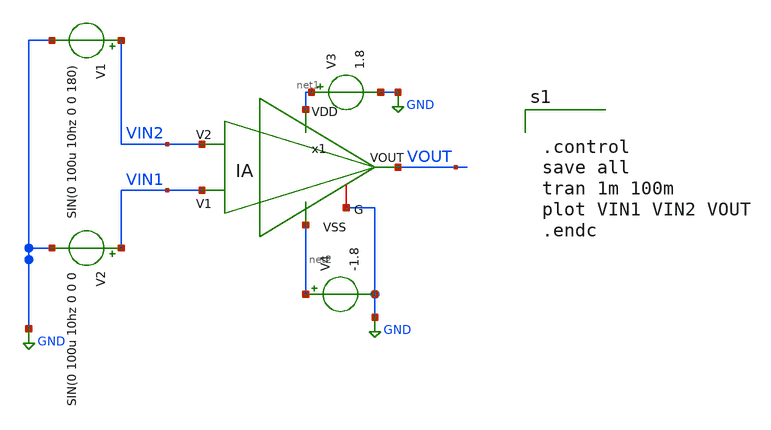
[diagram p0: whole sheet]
** sch_path: xschem/instropamp_inv_ss.sch
**.subckt instropamp_inv_ss
V1 VIN2 GND SIN(0 100u 10hz 0 0 180)
V2 VIN1 GND SIN(0 100u 10hz 0 0 0
V3 net1 GND 1.8
V4 net2 GND -1.8
x1 net1 net2 VOUT VIN1 VIN2 GND IA
**** begin user architecture code

** opencircuitdesign pdks install
.lib $::SKYWATER_MODELS/sky130.lib.spice ss




.control
save all
tran 1m 100m
plot VIN1 VIN2 VOUT
.endc


**** end user architecture code
**.ends

* expanding   symbol:  /foss/designs/chipalooza2024/sky130_hcmus_ip__instramp/xschem/IA.sym # of
*+ pins=6
** sym_path: /foss/designs/chipalooza2024/sky130_hcmus_ip__instramp/xschem/IA.sym
** sch_path: /foss/designs/chipalooza2024/sky130_hcmus_ip__instramp/xschem/IA.sch
.subckt IA VDD VSS VOUT V1 V2 G
*.opin VOUT
*.iopin G
*.ipin VDD
*.ipin VSS
*.ipin V1
*.ipin V2
XR1 net9 VOUT VSS sky130_fd_pr__res_high_po W=1 L=62 mult=1 m=1
XR4 net8 net1 VSS sky130_fd_pr__res_high_po W=1 L=62 mult=1 m=1
XR6 net12 G VSS sky130_fd_pr__res_high_po W=1 L=62 mult=1 m=1
XR8 net11 net2 VSS sky130_fd_pr__res_high_po W=1 L=62 mult=1 m=1
XR9 net3 net7 VSS sky130_fd_pr__res_high_po W=1 L=62 mult=1 m=1
XR12 net10 net4 VSS sky130_fd_pr__res_high_po W=1 L=62 mult=1 m=1
XR13 net5 net6 VSS sky130_fd_pr__res_high_po W=1 L=62 mult=1 m=1
x1 VDD VSS V2 net5 net3 opamp
x2 VDD VSS V1 net6 net4 opamp
x3 VDD VSS net2 net1 VOUT opamp
XR2 net7 net5 VSS sky130_fd_pr__res_high_po W=1 L=62 mult=1 m=1
XR3 net3 net8 VSS sky130_fd_pr__res_high_po W=1 L=62 mult=1 m=1
XR5 net1 net9 VSS sky130_fd_pr__res_high_po W=1 L=62 mult=1 m=1
XR7 net6 net10 VSS sky130_fd_pr__res_high_po W=1 L=62 mult=1 m=1
XR10 net4 net11 VSS sky130_fd_pr__res_high_po W=1 L=62 mult=1 m=1
XR11 net2 net12 VSS sky130_fd_pr__res_high_po W=1 L=62 mult=1 m=1
.ends


* expanding   symbol:  /foss/designs/chipalooza2024/sky130_hcmus_ip__instramp/xschem/opamp.sym # of
*+ pins=5
** sym_path: /foss/designs/chipalooza2024/sky130_hcmus_ip__instramp/xschem/opamp.sym
** sch_path: /foss/designs/chipalooza2024/sky130_hcmus_ip__instramp/xschem/opamp.sch
.subckt opamp VDD VSS V1 V2 VOUT
*.ipin VSS
*.ipin VDD
*.ipin V2
*.ipin V1
*.opin VOUT
XM2 net5 V2 net1 VSS sky130_fd_pr__nfet_g5v0d10v5 L=1 W=18 nf=1 ad='int((nf+1)/2) * W/nf * 0.29' as='int((nf+2)/2) * W/nf * 0.29'
+ pd='2*int((nf+1)/2) * (W/nf + 0.29)' ps='2*int((nf+2)/2) * (W/nf + 0.29)' nrd='0.29 / W' nrs='0.29 / W'
+ sa=0 sb=0 sd=0 mult=1 m=1
XM1 net6 net5 VDD VDD sky130_fd_pr__pfet_g5v0d10v5 L=1 W=30 nf=1 ad='int((nf+1)/2) * W/nf * 0.29' as='int((nf+2)/2) * W/nf * 0.29'
+ pd='2*int((nf+1)/2) * (W/nf + 0.29)' ps='2*int((nf+2)/2) * (W/nf + 0.29)' nrd='0.29 / W' nrs='0.29 / W'
+ sa=0 sb=0 sd=0 mult=1 m=1
XM4 net6 V1 net1 VSS sky130_fd_pr__nfet_g5v0d10v5 L=1 W=18 nf=1 ad='int((nf+1)/2) * W/nf * 0.29' as='int((nf+2)/2) * W/nf * 0.29'
+ pd='2*int((nf+1)/2) * (W/nf + 0.29)' ps='2*int((nf+2)/2) * (W/nf + 0.29)' nrd='0.29 / W' nrs='0.29 / W'
+ sa=0 sb=0 sd=0 mult=1 m=1
XM5 net1 net4 VSS VSS sky130_fd_pr__nfet_g5v0d10v5 L=1 W=15.171 nf=1 ad='int((nf+1)/2) * W/nf * 0.29'
+ as='int((nf+2)/2) * W/nf * 0.29' pd='2*int((nf+1)/2) * (W/nf + 0.29)' ps='2*int((nf+2)/2) * (W/nf + 0.29)'
+ nrd='0.29 / W' nrs='0.29 / W' sa=0 sb=0 sd=0 mult=1 m=1
XM6 VOUT net4 VSS VSS sky130_fd_pr__nfet_g5v0d10v5 L=1 W=19 nf=1 ad='int((nf+1)/2) * W/nf * 0.29' as='int((nf+2)/2) * W/nf * 0.29'
+ pd='2*int((nf+1)/2) * (W/nf + 0.29)' ps='2*int((nf+2)/2) * (W/nf + 0.29)' nrd='0.29 / W' nrs='0.29 / W'
+ sa=0 sb=0 sd=0 mult=1 m=1
XM7 net4 net4 VSS VSS sky130_fd_pr__nfet_g5v0d10v5 L=1 W=20 nf=1 ad='int((nf+1)/2) * W/nf * 0.29' as='int((nf+2)/2) * W/nf * 0.29'
+ pd='2*int((nf+1)/2) * (W/nf + 0.29)' ps='2*int((nf+2)/2) * (W/nf + 0.29)' nrd='0.29 / W' nrs='0.29 / W'
+ sa=0 sb=0 sd=0 mult=1 m=1
XM3 net5 net5 VDD VDD sky130_fd_pr__pfet_g5v0d10v5 L=1 W=30 nf=1 ad='int((nf+1)/2) * W/nf * 0.29' as='int((nf+2)/2) * W/nf * 0.29'
+ pd='2*int((nf+1)/2) * (W/nf + 0.29)' ps='2*int((nf+2)/2) * (W/nf + 0.29)' nrd='0.29 / W' nrs='0.29 / W'
+ sa=0 sb=0 sd=0 mult=1 m=1
XM8 VOUT net6 VDD VDD sky130_fd_pr__pfet_g5v0d10v5 L=1 W=38 nf=1 ad='int((nf+1)/2) * W/nf * 0.29' as='int((nf+2)/2) * W/nf * 0.29'
+ pd='2*int((nf+1)/2) * (W/nf + 0.29)' ps='2*int((nf+2)/2) * (W/nf + 0.29)' nrd='0.29 / W' nrs='0.29 / W'
+ sa=0 sb=0 sd=0 mult=2 m=2
XR3 net2 VDD VSS sky130_fd_pr__res_high_po W=1 L=30 mult=1 m=1
XR1 net3 net2 VSS sky130_fd_pr__res_high_po W=1 L=30 mult=1 m=1
XR2 net4 net3 VSS sky130_fd_pr__res_high_po W=1 L=30 mult=1 m=1
XR4 net7 VOUT VSS sky130_fd_pr__res_high_po W=1 L=5 mult=1 m=1
XC1 net7 net6 sky130_fd_pr__cap_mim_m3_1 W=5.5 L=10 MF=10 m=10
.ends

.GLOBAL GND
.end
